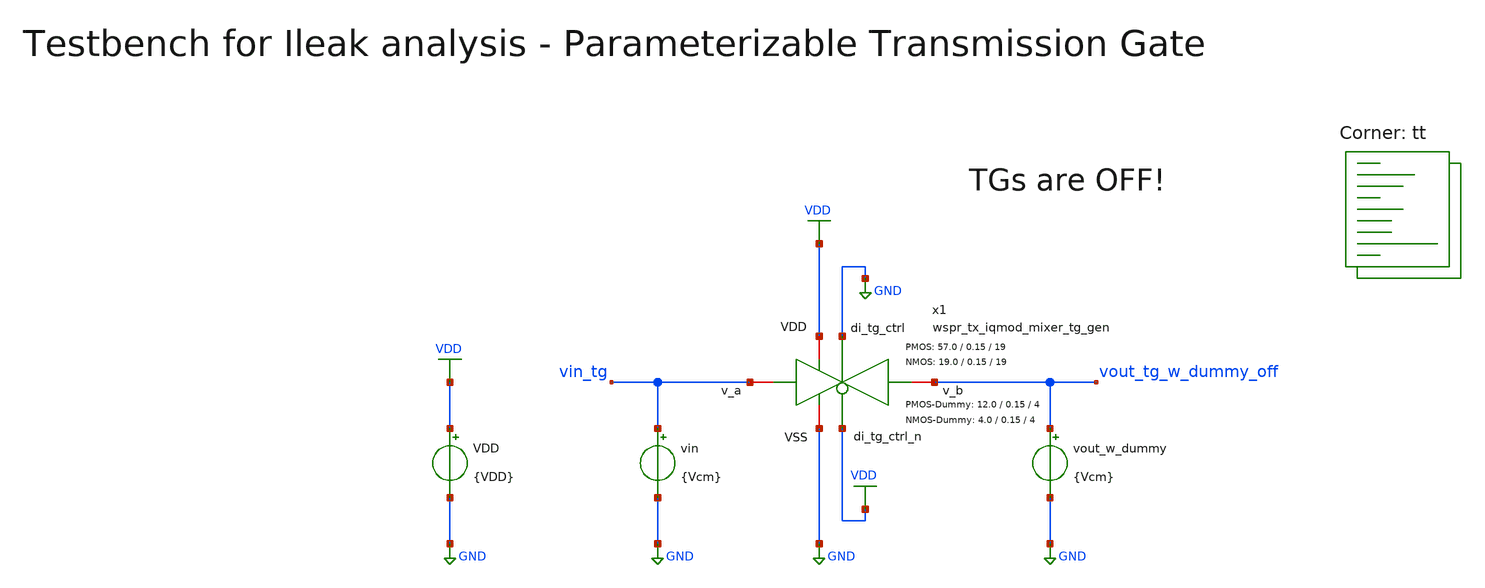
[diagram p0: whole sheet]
** sch_path: sky130/xschem/testbenches/wspr_tx_iqmod_mixer_tg_tb_dc_Ileak.sch
**.subckt wspr_tx_iqmod_mixer_tg_tb_dc_Ileak
VDD VDD GND {VDD}
vin vin_tg GND {Vcm}
vout_w_dummy vout_tg_w_dummy_off GND {Vcm}
x1 VDD GND GND vout_tg_w_dummy_off vin_tg VDD wspr_tx_iqmod_mixer_tg_gen W_P=57.0 L_P=0.15 NF_P=19
+ W_N=19.0 L_N=0.15 NF_N=19 W_P_D=12.0 L_P_D=0.15 NF_P_D=4 W_N_D=4.0 L_N_D=0.15 NF_N_D=4
**** begin user architecture code



.param VDD=1.8
.csparam VDD=VDD
.param Vcm=VDD/2
.csparam Vcm=Vcm
.param temp=27
.param Cload=10p
.options savecurrents klu method=gear reltol=1e-4 abstol=1e-15 gmin=1e-15
.control

save all

* Operating Point Analysis
op
remzerovec
write wspr_tx_iqmod_mixer_tg_tb_dc_Ileak.raw
set appendwrite
* =======================================

* DC Sweep Analysis LV with Dummy
dc vin 0 $&VDD 10m vout_w_dummy 0 $&VDD $&Vcm
write wspr_tx_iqmod_mixer_tg_tb_dc_Ileak.raw
set appendwrite

* Off-Leakage Current
let Ileak_w_dummy = i(vout_w_dummy)
plot Ileak_w_dummy
* =======================================

* Writing Data
set wr_singlescale
set wr_vecnames
let Ileak_w_dummy = dc1.Ileak_w_dummy
unset appendwrite
wrdata $PROJECT_PATH/python/plot_simulations/data/wspr_tx_iqmod_mixer_tg_tb_dc_Ileak.txt
+ v(Ileak_w_dummy)
* =======================================

*quit
.endc

.lib $::SKYWATER_MODELS/sky130.lib.spice tt
**** end user architecture code
**.ends
.GLOBAL GND
.GLOBAL VDD
.end
